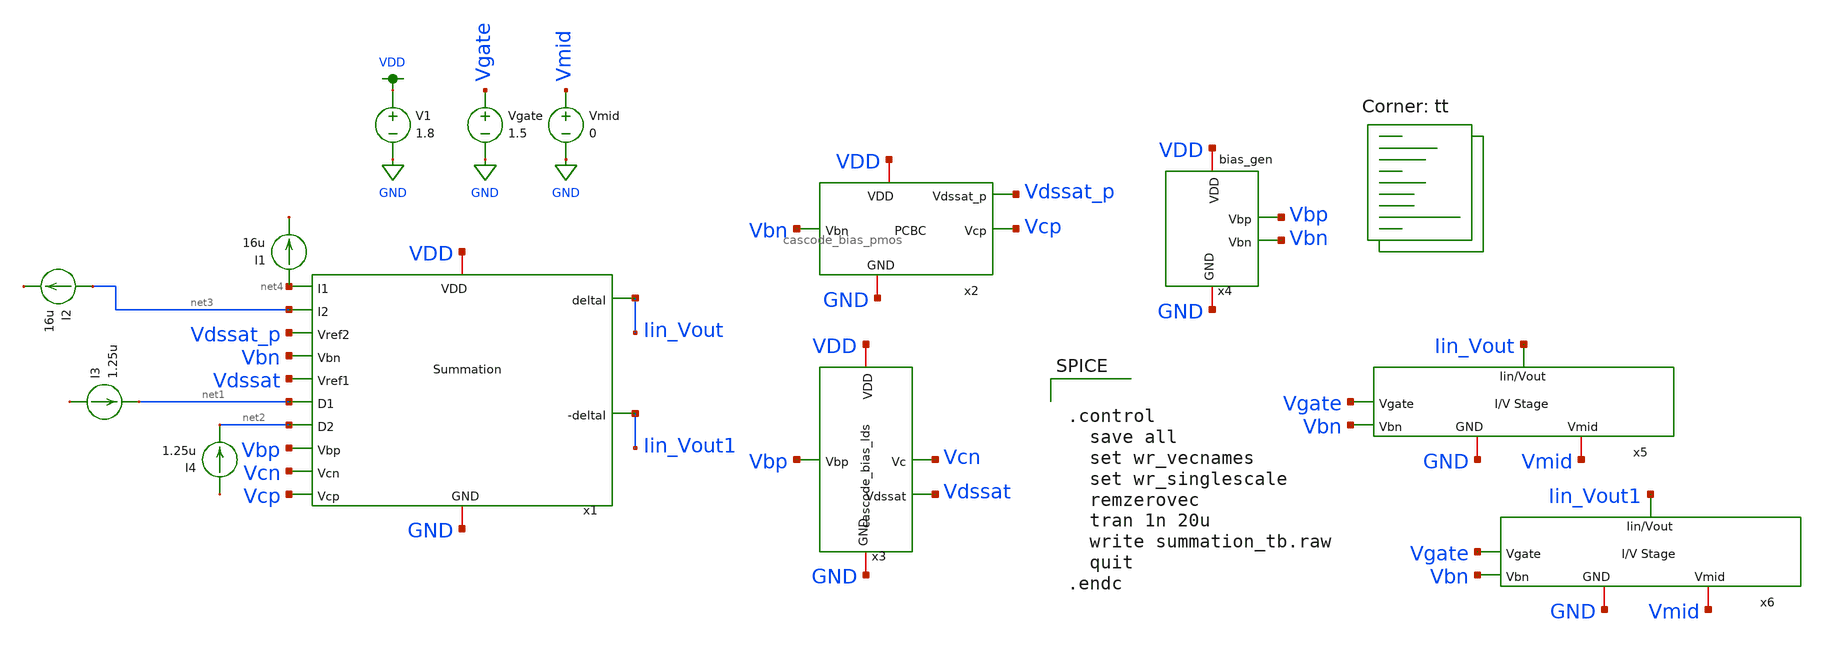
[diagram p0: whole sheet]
** sch_path: final/schematics/summation_tb.sch
**.subckt summation_tb
x1 VDD GND net4 net3 Vdssat_p Vbn Vdssat net1 net2 Iin_Vout Iin_Vout1 Vbp Vcn Vcp summation
x2 Vbn VDD GND Vcp Vdssat_p cascode_bias_pmos
x3 Vbp VDD Vcn GND Vdssat cascode_bias_lds
x4 VDD Vbp Vbn GND bias_gen
I1 net4 net5 16u
I2 net3 net6 16u
I3 net7 net1 1.25u
I4 net8 net2 1.25u
V1 VDD GND 1.8
x5 Iin_Vout Vgate Vmid Vbn GND IV_converter
x6 Iin_Vout1 Vgate Vmid Vbn GND IV_converter
Vgate Vgate GND 1.5
Vmid Vmid GND 0
**** begin user architecture code


.control
  save all
  set wr_vecnames
  set wr_singlescale
  remzerovec
  tran 1n 20u
  write summation_tb.raw
  quit
.endc


.lib $::SKYWATER_MODELS/sky130.lib.spice tt
**** end user architecture code
**.ends
.GLOBAL VDD
.GLOBAL GND
.end
